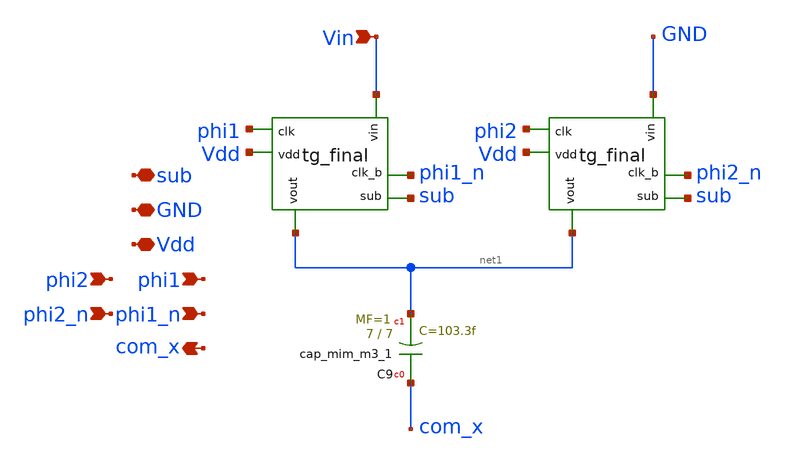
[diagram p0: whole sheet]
** sch_path: top/test/design/cap_switch_block.sch
**.subckt cap_switch_block Vin com_x phi1 phi1_n Vdd GND sub phi2 phi2_n
*.ipin Vin
*.opin com_x
*.ipin phi1
*.ipin phi1_n
*.iopin Vdd
*.iopin GND
*.iopin sub
*.ipin phi2
*.ipin phi2_n
XC9 com_x net1 sky130_fd_pr__cap_mim_m3_1 W=7 L=7 MF=1 m=1
x1 phi1 sub net1 Vin Vdd phi1_n tg_final
x2 phi2 sub net1 GND Vdd phi2_n tg_final
**.ends

* expanding   symbol:  /foss/designs/test/design/tg_final.sym # of pins=6
** sym_path: top/test/design/tg_final.sym
** sch_path: top/test/design/tg_final.sch
.subckt tg_final clk sub vout vin vdd clk_b
*.ipin clk
*.ipin vin
*.opin vout
*.ipin vdd
*.ipin sub
*.ipin clk_b
XM2 vout clk vin sub sky130_fd_pr__nfet_01v8 L=0.15 W=1 nf=1 ad='int((nf+1)/2) * W/nf * 0.29' as='int((nf+2)/2) * W/nf * 0.29'
+ pd='2*int((nf+1)/2) * (W/nf + 0.29)' ps='2*int((nf+2)/2) * (W/nf + 0.29)' nrd='0.29 / W' nrs='0.29 / W'
+ sa=0 sb=0 sd=0 mult=1 m=1
XM1 vout clk_b vin vdd sky130_fd_pr__pfet_01v8 L=0.15 W=1 nf=1 ad='int((nf+1)/2) * W/nf * 0.29' as='int((nf+2)/2) * W/nf * 0.29'
+ pd='2*int((nf+1)/2) * (W/nf + 0.29)' ps='2*int((nf+2)/2) * (W/nf + 0.29)' nrd='0.29 / W' nrs='0.29 / W'
+ sa=0 sb=0 sd=0 mult=1 m=1
.ends

.end
